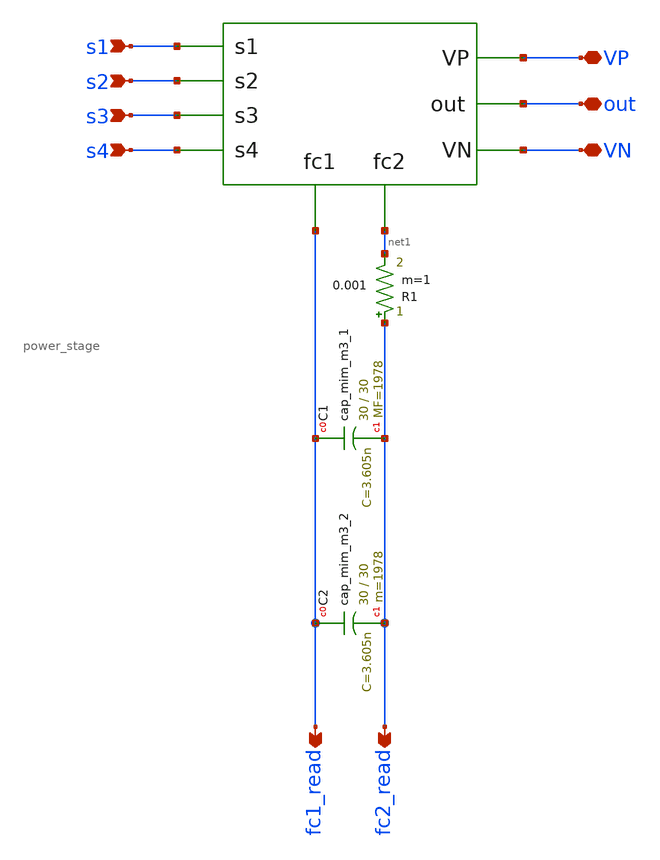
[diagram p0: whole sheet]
** sch_path: xschem/hierarchy_sch/converter.sch
**.subckt converter s1 s2 s3 s4 VP VN fc1_read fc2_read out
*.ipin s1
*.ipin s2
*.ipin s3
*.ipin s4
*.iopin VP
*.iopin VN
*.opin fc1_read
*.opin fc2_read
*.iopin out
X1v s1 s2 s3 s4 fc1_read net1 out VP VN power_stage
R1 fc2_read net1 0.001 m=1
XC1 fc1_read fc2_read sky130_fd_pr__cap_mim_m3_1 W=30 L=30 MF=1978 m=1978
XC2 fc1_read fc2_read sky130_fd_pr__cap_mim_m3_2 W=30 L=30 MF=1978 m=1978
**.ends

* expanding   symbol:  personal/3LFCC_AC3E/xschem/hierarchy_sch/power_stage.sym # of pins=9
** sym_path: xschem/hierarchy_sch/power_stage.sym
** sch_path: xschem/hierarchy_sch/power_stage.sch
.subckt power_stage s1 s2 s3 s4 fc1 fc2 out VP VN
*.ipin s1
*.ipin s2
*.ipin s3
*.ipin s4
*.iopin VP
*.iopin VN
*.opin out
*.opin fc1
*.opin fc2
X1 s2 fc1 s1 VP out transistor_group_one
X2 s4 fc2 s3 out VN transistor_group_two
.ends


* expanding   symbol:  personal/3LFCC_AC3E/xschem/hierarchy_sch/transistor_group_one.sym # of pins=5
** sym_path: xschem/hierarchy_sch/transistor_group_one.sym
** sch_path: xschem/hierarchy_sch/transistor_group_one.sch
.subckt transistor_group_one s2 fc1 s1 VP out
*.iopin VP
*.ipin s1
*.ipin s2
*.opin fc1
*.iopin out
XM3 out s2 fc1 fc1 sky130_fd_pr__pfet_g5v0d10v5 L=0.5 W=4.38 nf=1 ad='int((nf+1)/2) * W/nf * 0.29' as='int((nf+2)/2) * W/nf * 0.29'
+ pd='2*int((nf+1)/2) * (W/nf + 0.29)' ps='2*int((nf+2)/2) * (W/nf + 0.29)' nrd='0.29 / W' nrs='0.29 / W'
+ sa=0 sb=0 sd=0 mult=4506 m=4506
XM4 fc1 s1 VP VP sky130_fd_pr__pfet_g5v0d10v5 L=0.5 W=4.38 nf=1 ad='int((nf+1)/2) * W/nf * 0.29' as='int((nf+2)/2) * W/nf * 0.29'
+ pd='2*int((nf+1)/2) * (W/nf + 0.29)' ps='2*int((nf+2)/2) * (W/nf + 0.29)' nrd='0.29 / W' nrs='0.29 / W'
+ sa=0 sb=0 sd=0 mult=4506 m=4506
.ends


* expanding   symbol:  personal/3LFCC_AC3E/xschem/hierarchy_sch/transistor_group_two.sym # of pins=5
** sym_path: xschem/hierarchy_sch/transistor_group_two.sym
** sch_path: xschem/hierarchy_sch/transistor_group_two.sch
.subckt transistor_group_two s4 fc2 s3 out VN
*.iopin out
*.ipin s3
*.ipin s4
*.opin fc2
*.iopin VN
XM1 out s3 fc2 fc2 sky130_fd_pr__nfet_g5v0d10v5 L=0.5 W=4.38 nf=1 ad='int((nf+1)/2) * W/nf * 0.29' as='int((nf+2)/2) * W/nf * 0.29'
+ pd='2*int((nf+1)/2) * (W/nf + 0.29)' ps='2*int((nf+2)/2) * (W/nf + 0.29)' nrd='0.29 / W' nrs='0.29 / W'
+ sa=0 sb=0 sd=0 mult=2520 m=2520
XM2 fc2 s4 VN VN sky130_fd_pr__nfet_g5v0d10v5 L=0.5 W=4.38 nf=1 ad='int((nf+1)/2) * W/nf * 0.29' as='int((nf+2)/2) * W/nf * 0.29'
+ pd='2*int((nf+1)/2) * (W/nf + 0.29)' ps='2*int((nf+2)/2) * (W/nf + 0.29)' nrd='0.29 / W' nrs='0.29 / W'
+ sa=0 sb=0 sd=0 mult=2520 m=2520
.ends

.end
